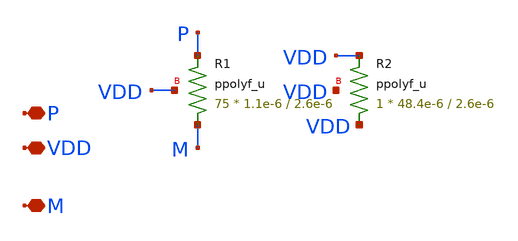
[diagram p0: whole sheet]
** sch_path: Clock_Generator_PAKISTAN_06/Schematics/Res_74k.sch
**.subckt Res_74k P VDD M
*.iopin P
*.iopin VDD
*.iopin M
XR1 M P VDD ppolyf_u r_width=1.1e-6 r_length=2.6e-6 m=75
XR2 VDD VDD VDD ppolyf_u r_width=48.4e-6 r_length=2.6e-6 m=1
**.ends
.end
